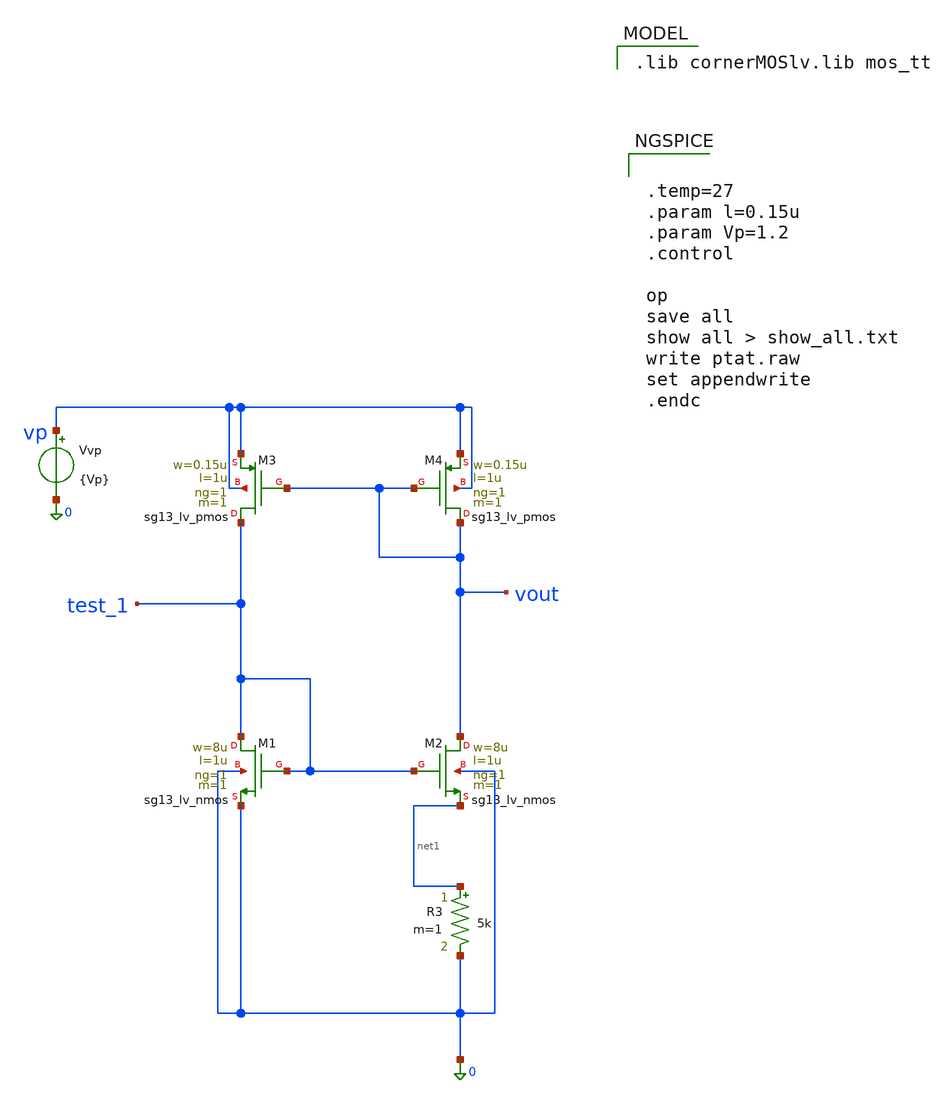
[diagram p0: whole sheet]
** sch_path: PLL0663-main/schematic/xschem/charge_pump/vbias/ptat.sch
**.subckt ptat
XM1 test_1 test_1 0 0 sg13_lv_nmos w=8u l=1u ng=1 m=1 mm_ok=1
XM3 test_1 vout vp vp sg13_lv_pmos w=0.15u l=1u ng=1 m=1 mm_ok=1
XM2 vout test_1 net1 0 sg13_lv_nmos w=8u l=1u ng=1 m=1 mm_ok=1
XM4 vout vout vp vp sg13_lv_pmos w=0.15u l=1u ng=1 m=1 mm_ok=1
R3 net1 0 5k m=1
Vvp vp 0 {Vp}
**** begin user architecture code
 .lib cornerMOSlv.lib mos_tt



.temp=27
.param l=0.15u
.param Vp=1.2
.control

op
save all
show all > show_all.txt
write ptat.raw
set appendwrite
.endc


**** end user architecture code
**.ends
.end
